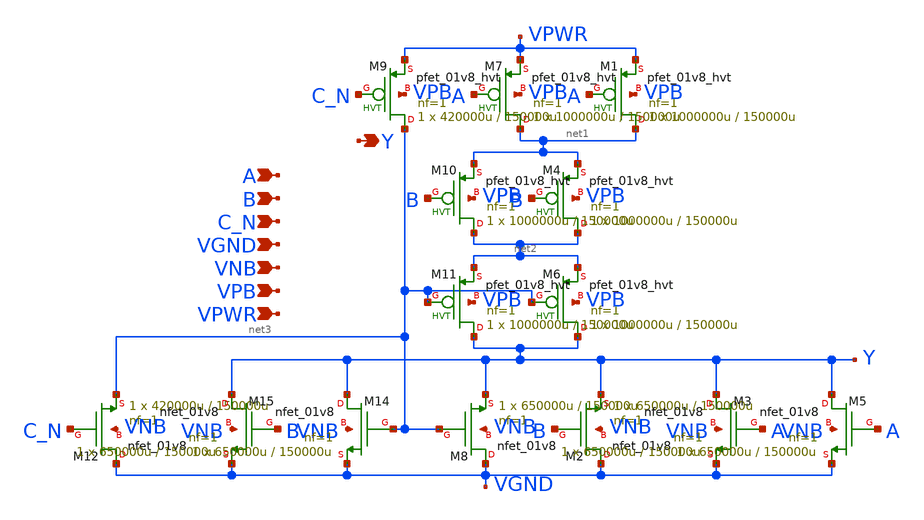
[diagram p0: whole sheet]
** sch_path: schematics/nor3b/sky130_fd_sc_hd__nor3b_2.sch
**.subckt sky130_fd_sc_hd__nor3b_2 A B VGND VNB VPB VPWR Y C_N
*.ipin A
*.ipin B
*.ipin VGND
*.ipin VNB
*.ipin VPB
*.ipin VPWR
*.opin Y
*.ipin C_N
XM1 net1 A VPWR VPB sky130_fd_pr__pfet_01v8_hvt L=150000u W=1000000u nf=1 ad='int((1 + 1)/2) * 1000000u / 1 * 0.29'
+ as='int((1 + 2)/2) * 1000000u / 1 * 0.29' pd='2*int((1 + 1)/2) * (1000000u / 1 + 0.29)' ps='2*int((1 + 2)/2) * (1000000u / 1 + 0.29)'
+ nrd='0.29 / 1000000u ' nrs='0.29 / 1000000u ' sa=0 sb=0 sd=0 mult=1 m=1
XM2 VGND B Y VNB sky130_fd_pr__nfet_01v8 L=150000u W=650000u nf=1 ad='int((1 + 1)/2) * 650000u / 1 * 0.29'
+ as='int((1 + 2)/2) * 650000u / 1 * 0.29' pd='2*int((1 + 1)/2) * (650000u / 1 + 0.29)' ps='2*int((1 + 2)/2) * (650000u / 1 + 0.29)'
+ nrd='0.29 / 650000u ' nrs='0.29 / 650000u ' sa=0 sb=0 sd=0 mult=1 m=1
XM7 net1 A VPWR VPB sky130_fd_pr__pfet_01v8_hvt L=150000u W=1000000u nf=1 ad='int((1 + 1)/2) * 1000000u / 1 * 0.29'
+ as='int((1 + 2)/2) * 1000000u / 1 * 0.29' pd='2*int((1 + 1)/2) * (1000000u / 1 + 0.29)' ps='2*int((1 + 2)/2) * (1000000u / 1 + 0.29)'
+ nrd='0.29 / 1000000u ' nrs='0.29 / 1000000u ' sa=0 sb=0 sd=0 mult=1 m=1
XM8 VGND net3 Y VNB sky130_fd_pr__nfet_01v8 L=150000u W=650000u nf=1 ad='int((1 + 1)/2) * 650000u / 1 * 0.29'
+ as='int((1 + 2)/2) * 650000u / 1 * 0.29' pd='2*int((1 + 1)/2) * (650000u / 1 + 0.29)' ps='2*int((1 + 2)/2) * (650000u / 1 + 0.29)'
+ nrd='0.29 / 650000u ' nrs='0.29 / 650000u ' sa=0 sb=0 sd=0 mult=1 m=1
XM5 Y A VGND VNB sky130_fd_pr__nfet_01v8 L=150000u W=650000u nf=1 ad='int((1 + 1)/2) * 650000u / 1 * 0.29'
+ as='int((1 + 2)/2) * 650000u / 1 * 0.29' pd='2*int((1 + 1)/2) * (650000u / 1 + 0.29)' ps='2*int((1 + 2)/2) * (650000u / 1 + 0.29)'
+ nrd='0.29 / 650000u ' nrs='0.29 / 650000u ' sa=0 sb=0 sd=0 mult=1 m=1
XM3 Y A VGND VNB sky130_fd_pr__nfet_01v8 L=150000u W=650000u nf=1 ad='int((1 + 1)/2) * 650000u / 1 * 0.29'
+ as='int((1 + 2)/2) * 650000u / 1 * 0.29' pd='2*int((1 + 1)/2) * (650000u / 1 + 0.29)' ps='2*int((1 + 2)/2) * (650000u / 1 + 0.29)'
+ nrd='0.29 / 650000u ' nrs='0.29 / 650000u ' sa=0 sb=0 sd=0 mult=1 m=1
XM4 net2 B net1 VPB sky130_fd_pr__pfet_01v8_hvt L=150000u W=1000000u nf=1 ad='int((1 + 1)/2) * 1000000u / 1 * 0.29'
+ as='int((1 + 2)/2) * 1000000u / 1 * 0.29' pd='2*int((1 + 1)/2) * (1000000u / 1 + 0.29)' ps='2*int((1 + 2)/2) * (1000000u / 1 + 0.29)'
+ nrd='0.29 / 1000000u ' nrs='0.29 / 1000000u ' sa=0 sb=0 sd=0 mult=1 m=1
XM6 Y net3 net2 VPB sky130_fd_pr__pfet_01v8_hvt L=150000u W=1000000u nf=1 ad='int((1 + 1)/2) * 1000000u / 1 * 0.29'
+ as='int((1 + 2)/2) * 1000000u / 1 * 0.29' pd='2*int((1 + 1)/2) * (1000000u / 1 + 0.29)' ps='2*int((1 + 2)/2) * (1000000u / 1 + 0.29)'
+ nrd='0.29 / 1000000u ' nrs='0.29 / 1000000u ' sa=0 sb=0 sd=0 mult=1 m=1
XM9 net3 C_N VPWR VPB sky130_fd_pr__pfet_01v8_hvt L=150000u W=420000u nf=1 ad='int((1 + 1)/2) * 420000u / 1 * 0.29'
+ as='int((1 + 2)/2) * 420000u / 1 * 0.29' pd='2*int((1 + 1)/2) * (420000u / 1 + 0.29)' ps='2*int((1 + 2)/2) * (420000u / 1 + 0.29)'
+ nrd='0.29 / 420000u ' nrs='0.29 / 420000u ' sa=0 sb=0 sd=0 mult=1 m=1
XM10 net2 B net1 VPB sky130_fd_pr__pfet_01v8_hvt L=150000u W=1000000u nf=1 ad='int((1 + 1)/2) * 1000000u / 1 * 0.29'
+ as='int((1 + 2)/2) * 1000000u / 1 * 0.29' pd='2*int((1 + 1)/2) * (1000000u / 1 + 0.29)' ps='2*int((1 + 2)/2) * (1000000u / 1 + 0.29)'
+ nrd='0.29 / 1000000u ' nrs='0.29 / 1000000u ' sa=0 sb=0 sd=0 mult=1 m=1
XM11 Y net3 net2 VPB sky130_fd_pr__pfet_01v8_hvt L=150000u W=1000000u nf=1 ad='int((1 + 1)/2) * 1000000u / 1 * 0.29'
+ as='int((1 + 2)/2) * 1000000u / 1 * 0.29' pd='2*int((1 + 1)/2) * (1000000u / 1 + 0.29)' ps='2*int((1 + 2)/2) * (1000000u / 1 + 0.29)'
+ nrd='0.29 / 1000000u ' nrs='0.29 / 1000000u ' sa=0 sb=0 sd=0 mult=1 m=1
XM12 VGND C_N net3 VNB sky130_fd_pr__nfet_01v8 L=150000u W=420000u nf=1 ad='int((1 + 1)/2) * 420000u / 1 * 0.29'
+ as='int((1 + 2)/2) * 420000u / 1 * 0.29' pd='2*int((1 + 1)/2) * (420000u / 1 + 0.29)' ps='2*int((1 + 2)/2) * (420000u / 1 + 0.29)'
+ nrd='0.29 / 420000u ' nrs='0.29 / 420000u ' sa=0 sb=0 sd=0 mult=1 m=1
XM14 Y net3 VGND VNB sky130_fd_pr__nfet_01v8 L=150000u W=650000u nf=1 ad='int((1 + 1)/2) * 650000u / 1 * 0.29'
+ as='int((1 + 2)/2) * 650000u / 1 * 0.29' pd='2*int((1 + 1)/2) * (650000u / 1 + 0.29)' ps='2*int((1 + 2)/2) * (650000u / 1 + 0.29)'
+ nrd='0.29 / 650000u ' nrs='0.29 / 650000u ' sa=0 sb=0 sd=0 mult=1 m=1
XM15 Y B VGND VNB sky130_fd_pr__nfet_01v8 L=150000u W=650000u nf=1 ad='int((1 + 1)/2) * 650000u / 1 * 0.29'
+ as='int((1 + 2)/2) * 650000u / 1 * 0.29' pd='2*int((1 + 1)/2) * (650000u / 1 + 0.29)' ps='2*int((1 + 2)/2) * (650000u / 1 + 0.29)'
+ nrd='0.29 / 650000u ' nrs='0.29 / 650000u ' sa=0 sb=0 sd=0 mult=1 m=1
**.ends
.end
